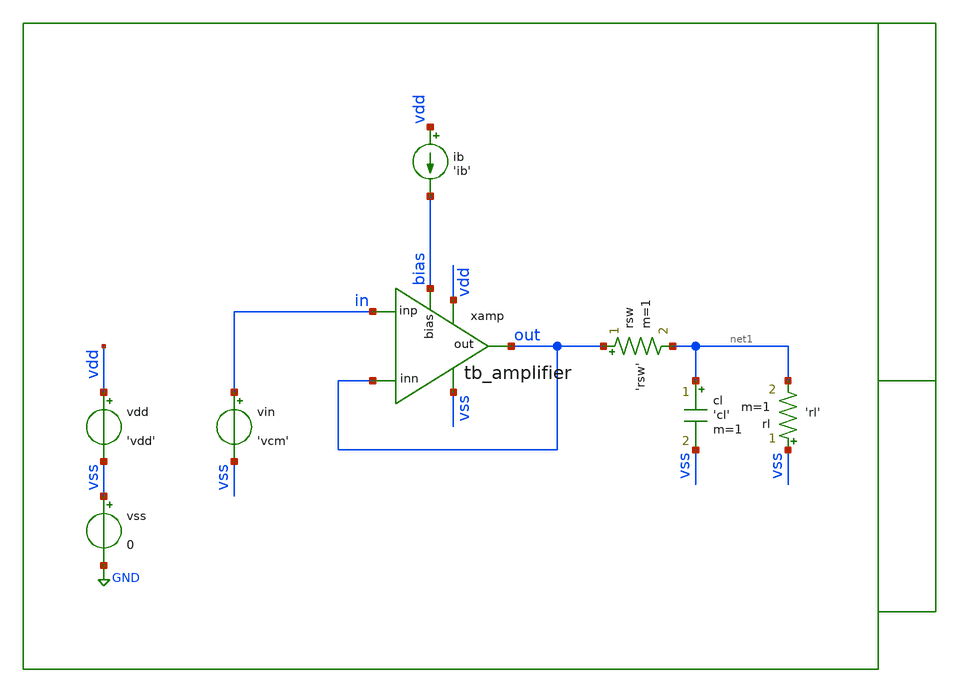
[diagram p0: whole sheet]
** sch_path: xschem/tb/testbuffer/tb_amplifier/dc_tb_amplifier_icmr.sch
**.subckt dc_tb_amplifier_icmr
vin in vss 'vcm'
ib vdd bias 'ib'
vdd vdd vss 'vdd'
vss vss GND 0
xamp vdd out in out vss bias tb_amplifier
cl net1 vss 'cl' m=1
rl vss net1 'rl' m=1
rsw out net1 'rsw' m=1
**** begin user architecture code
 *Control

.param vdd=3.3
.param vcm='vdd/2'
.param ib=5u
.param cl=1p
.param rl=1e6
.param rsw=1

.csparam ctrlvdd = 'vdd'

.control
save all

* vout/vin = Avol/(1+Avol*Beta)

let gain_threshold = 60
let avol = 10^(gain_threshold/20)
let threshold = avol/(1+avol)

let vstart = 0.3
let vend   = 1.0
dc vin $&vstart $&vend 0.01
let ratio = v(out)/v(in)
meas dc vin_min when ratio=threshold rise=1
let icmr_min = vin_min
print vin_min
print icmr_min

let vstart = $&ctrlvdd - 0.3
let vend   = $&ctrlvdd
dc vin $&vstart $&vend 0.01
let ratio = v(out)/v(in)
meas dc vin_max when ratio=threshold fall=1
print vin_max
let icmr_max = $&ctrlvdd - vin_max
print icmr_max

setplot dc1
gnuplot p1 ratio
setplot dc2
gnuplot p2 ratio

.endc

 * Model Corners

.include $::CORNERS/ngspice/tt.spice
*.include $::CORNERS/ngspice/ff.spice
*.include $::CORNERS/ngspice/ss.spice
*.include $::CORNERS/ngspice/sf.spice
*.include $::CORNERS/ngspice/fs.spice

**** end user architecture code
**.ends

* expanding   symbol:  sch/testbuffer/tb_amplifier/tb_amplifier.sym # of pins=6
** sym_path: xschem/sch/testbuffer/tb_amplifier/tb_amplifier.sym
** sch_path: xschem/sch/testbuffer/tb_amplifier/tb_amplifier.sch
.subckt tb_amplifier vdd out inp inn vss bias
*.ipin inn
*.ipin inp
*.opin out
*.iopin bias
*.iopin vdd
*.iopin vss
XM3 mirr mirr vdd vdd pfet_06v0 L=4u W=16u nf=2 ad='int((nf+1)/2) * W/nf * 0.18u' as='int((nf+2)/2) * W/nf * 0.18u'
+ pd='2*int((nf+1)/2) * (W/nf + 0.18u)' ps='2*int((nf+2)/2) * (W/nf + 0.18u)' nrd='0.18u / W' nrs='0.18u / W'
+ sa=0 sb=0 sd=0 m=2 par=2
XM4 comp mirr vdd vdd pfet_06v0 L=4u W=16u nf=2 ad='int((nf+1)/2) * W/nf * 0.18u' as='int((nf+2)/2) * W/nf * 0.18u'
+ pd='2*int((nf+1)/2) * (W/nf + 0.18u)' ps='2*int((nf+2)/2) * (W/nf + 0.18u)' nrd='0.18u / W' nrs='0.18u / W'
+ sa=0 sb=0 sd=0 m=2 par=2
XM2 comp inp vcm vss nfet_06v0 L=2u W=16u nf=2 ad='int((nf+1)/2) * W/nf * 0.18u' as='int((nf+2)/2) * W/nf * 0.18u'
+ pd='2*int((nf+1)/2) * (W/nf + 0.18u)' ps='2*int((nf+2)/2) * (W/nf + 0.18u)' nrd='0.18u / W' nrs='0.18u / W'
+ sa=0 sb=0 sd=0 m=2 par=2
XM1 mirr inn vcm vss nfet_06v0 L=2u W=16u nf=2 ad='int((nf+1)/2) * W/nf * 0.18u' as='int((nf+2)/2) * W/nf * 0.18u'
+ pd='2*int((nf+1)/2) * (W/nf + 0.18u)' ps='2*int((nf+2)/2) * (W/nf + 0.18u)' nrd='0.18u / W' nrs='0.18u / W'
+ sa=0 sb=0 sd=0 m=2 par=2
XM5 vcm bias vss vss nfet_06v0 L=1u W=16u nf=2 ad='int((nf+1)/2) * W/nf * 0.18u' as='int((nf+2)/2) * W/nf * 0.18u'
+ pd='2*int((nf+1)/2) * (W/nf + 0.18u)' ps='2*int((nf+2)/2) * (W/nf + 0.18u)' nrd='0.18u / W' nrs='0.18u / W'
+ sa=0 sb=0 sd=0 m=2 par=2
XM6 out bias vss vss nfet_06v0 L=1u W=16u nf=2 ad='int((nf+1)/2) * W/nf * 0.18u' as='int((nf+2)/2) * W/nf * 0.18u'
+ pd='2*int((nf+1)/2) * (W/nf + 0.18u)' ps='2*int((nf+2)/2) * (W/nf + 0.18u)' nrd='0.18u / W' nrs='0.18u / W'
+ sa=0 sb=0 sd=0 m=12 par=12
XM7 out comp vdd vdd pfet_06v0 L=1u W=96u nf=12 ad='int((nf+1)/2) * W/nf * 0.18u' as='int((nf+2)/2) * W/nf * 0.18u'
+ pd='2*int((nf+1)/2) * (W/nf + 0.18u)' ps='2*int((nf+2)/2) * (W/nf + 0.18u)' nrd='0.18u / W' nrs='0.18u / W'
+ sa=0 sb=0 sd=0 m=1 par=1
XMB1 bias bias vss vss nfet_06v0 L=1u W=16u nf=2 ad='int((nf+1)/2) * W/nf * 0.18u' as='int((nf+2)/2) * W/nf * 0.18u'
+ pd='2*int((nf+1)/2) * (W/nf + 0.18u)' ps='2*int((nf+2)/2) * (W/nf + 0.18u)' nrd='0.18u / W' nrs='0.18u / W'
+ sa=0 sb=0 sd=0 m=2 par=2
XMB2 vbm bias vss vss nfet_06v0 L=1u W=16u nf=2 ad='int((nf+1)/2) * W/nf * 0.18u' as='int((nf+2)/2) * W/nf * 0.18u'
+ pd='2*int((nf+1)/2) * (W/nf + 0.18u)' ps='2*int((nf+2)/2) * (W/nf + 0.18u)' nrd='0.18u / W' nrs='0.18u / W'
+ sa=0 sb=0 sd=0 m=2 par=2
XMB3 vbm vbm vbt vdd pfet_06v0 L=1u W=16u nf=2 ad='int((nf+1)/2) * W/nf * 0.18u' as='int((nf+2)/2) * W/nf * 0.18u'
+ pd='2*int((nf+1)/2) * (W/nf + 0.18u)' ps='2*int((nf+2)/2) * (W/nf + 0.18u)' nrd='0.18u / W' nrs='0.18u / W'
+ sa=0 sb=0 sd=0 m=1 par=1
XMB4 vbt vbt vdd vdd pfet_06v0 L=1u W=16u nf=2 ad='int((nf+1)/2) * W/nf * 0.18u' as='int((nf+2)/2) * W/nf * 0.18u'
+ pd='2*int((nf+1)/2) * (W/nf + 0.18u)' ps='2*int((nf+2)/2) * (W/nf + 0.18u)' nrd='0.18u / W' nrs='0.18u / W'
+ sa=0 sb=0 sd=0 m=1 par=1
XRCC gc comp vdd ppolyf_u_1k_6p0 r_width=2e-6 r_length=38e-6 s=1 m=1
XMDUM1 vss vss vss vss nfet_06v0 L=2u W=16u nf=2 ad='int((nf+1)/2) * W/nf * 0.18u' as='int((nf+2)/2) * W/nf * 0.18u'
+ pd='2*int((nf+1)/2) * (W/nf + 0.18u)' ps='2*int((nf+2)/2) * (W/nf + 0.18u)' nrd='0.18u / W' nrs='0.18u / W'
+ sa=0 sb=0 sd=0 m=2 par=2
XMDUM2 vdd vdd vdd vdd pfet_06v0 L=4u W=16u nf=2 ad='int((nf+1)/2) * W/nf * 0.18u' as='int((nf+2)/2) * W/nf * 0.18u'
+ pd='2*int((nf+1)/2) * (W/nf + 0.18u)' ps='2*int((nf+2)/2) * (W/nf + 0.18u)' nrd='0.18u / W' nrs='0.18u / W'
+ sa=0 sb=0 sd=0 m=4 par=4
XC1 out gc cap_mim_2f0_m4m5_noshield c_width=30e-6 c_length=30e-6 m=1
.ends

.GLOBAL GND
.end
